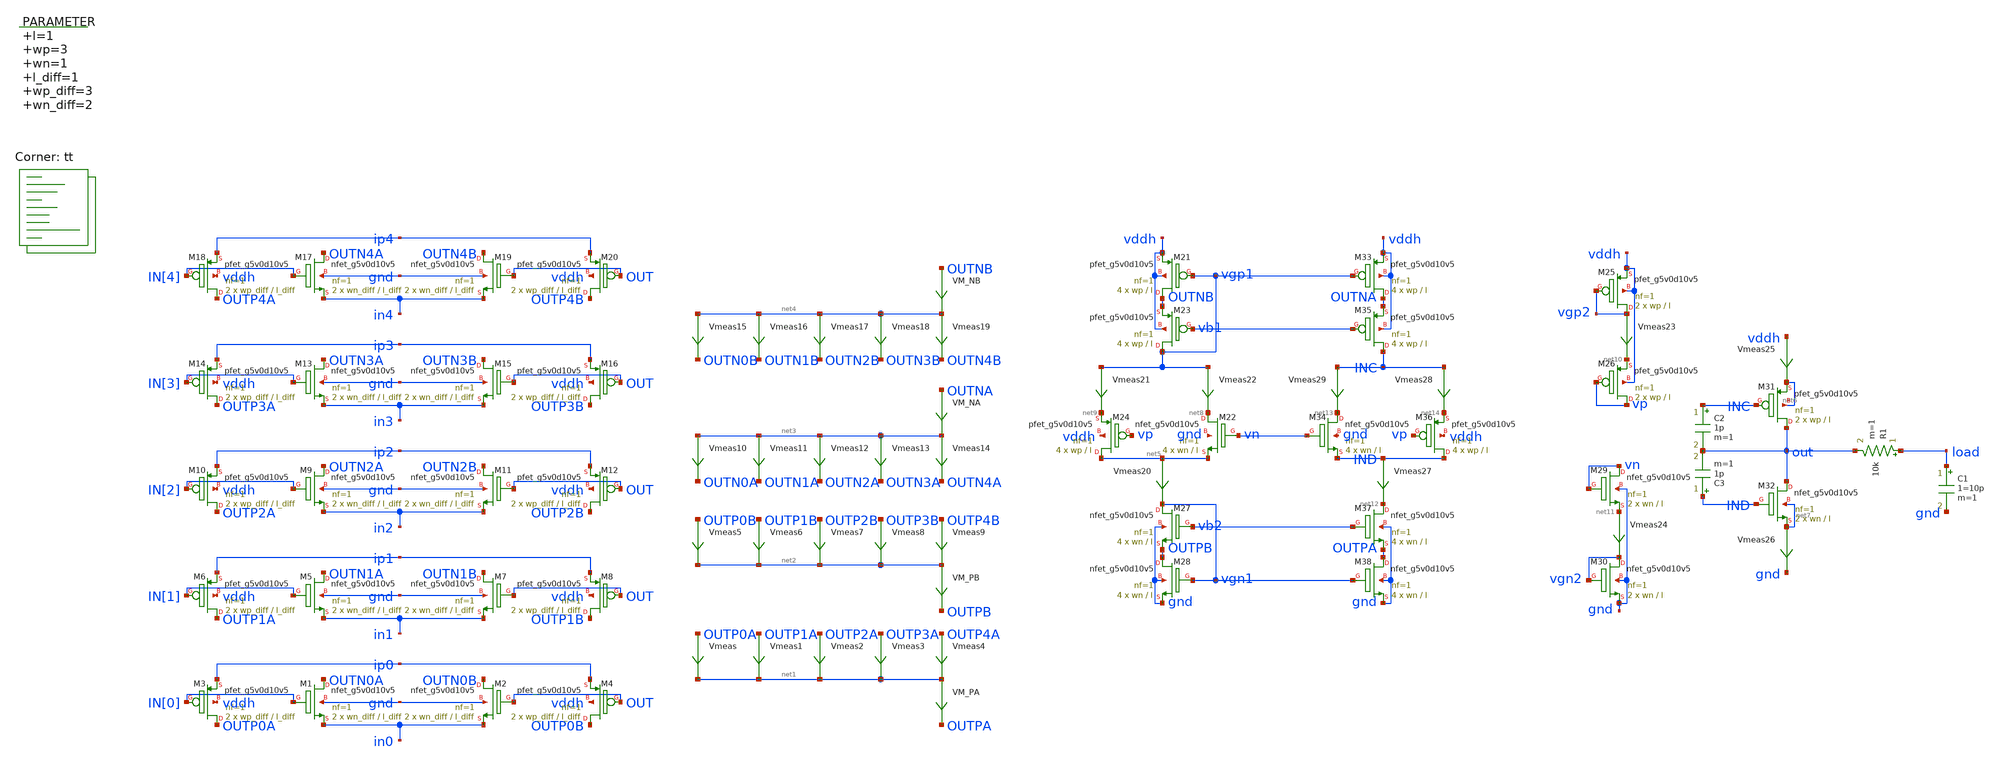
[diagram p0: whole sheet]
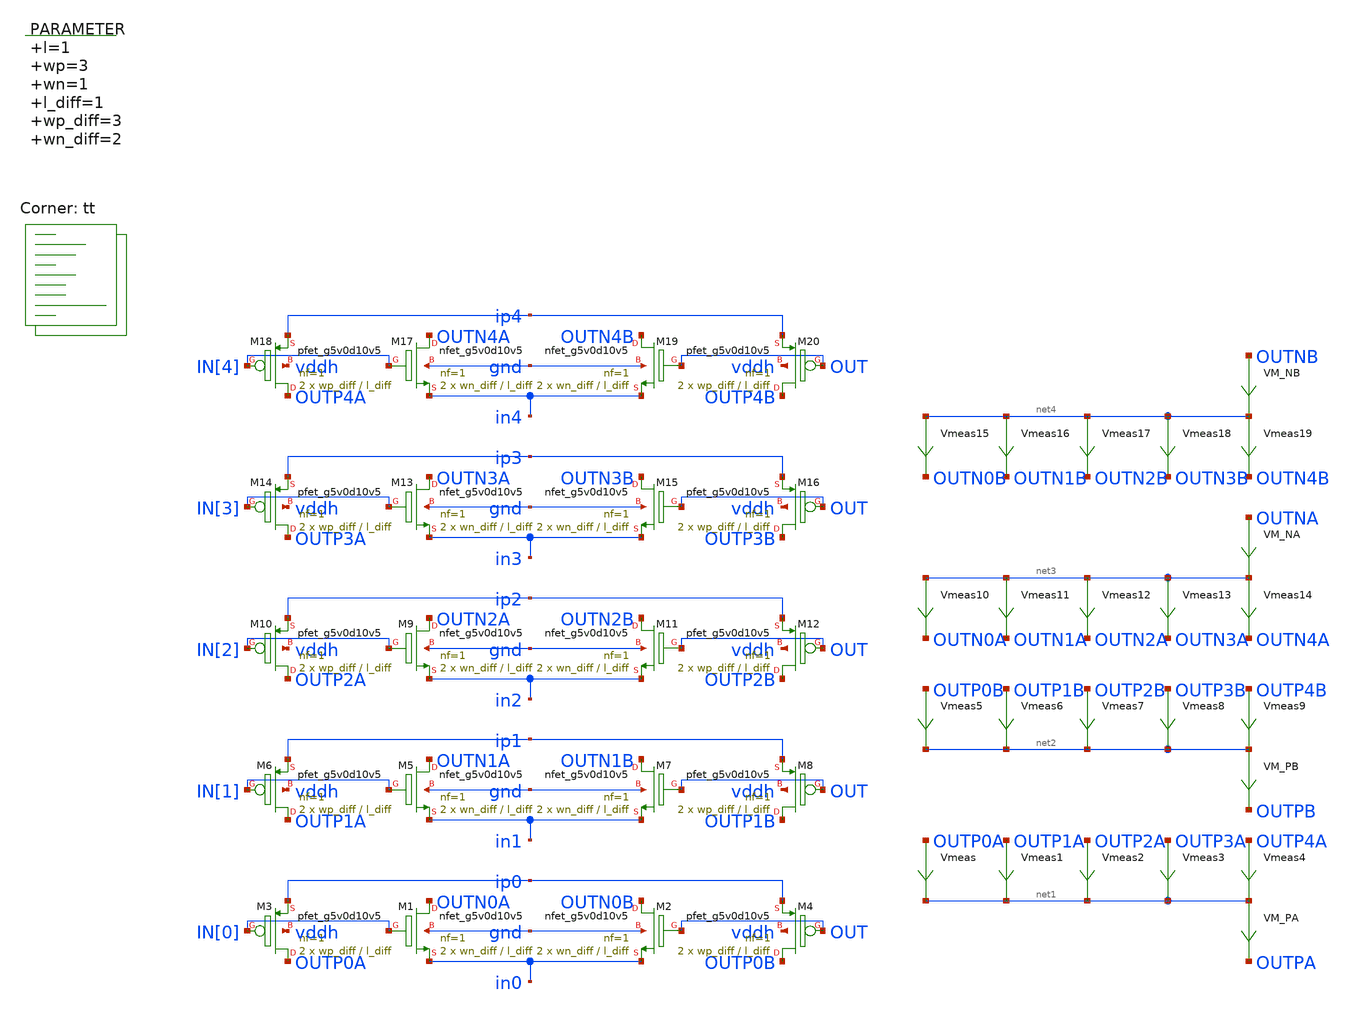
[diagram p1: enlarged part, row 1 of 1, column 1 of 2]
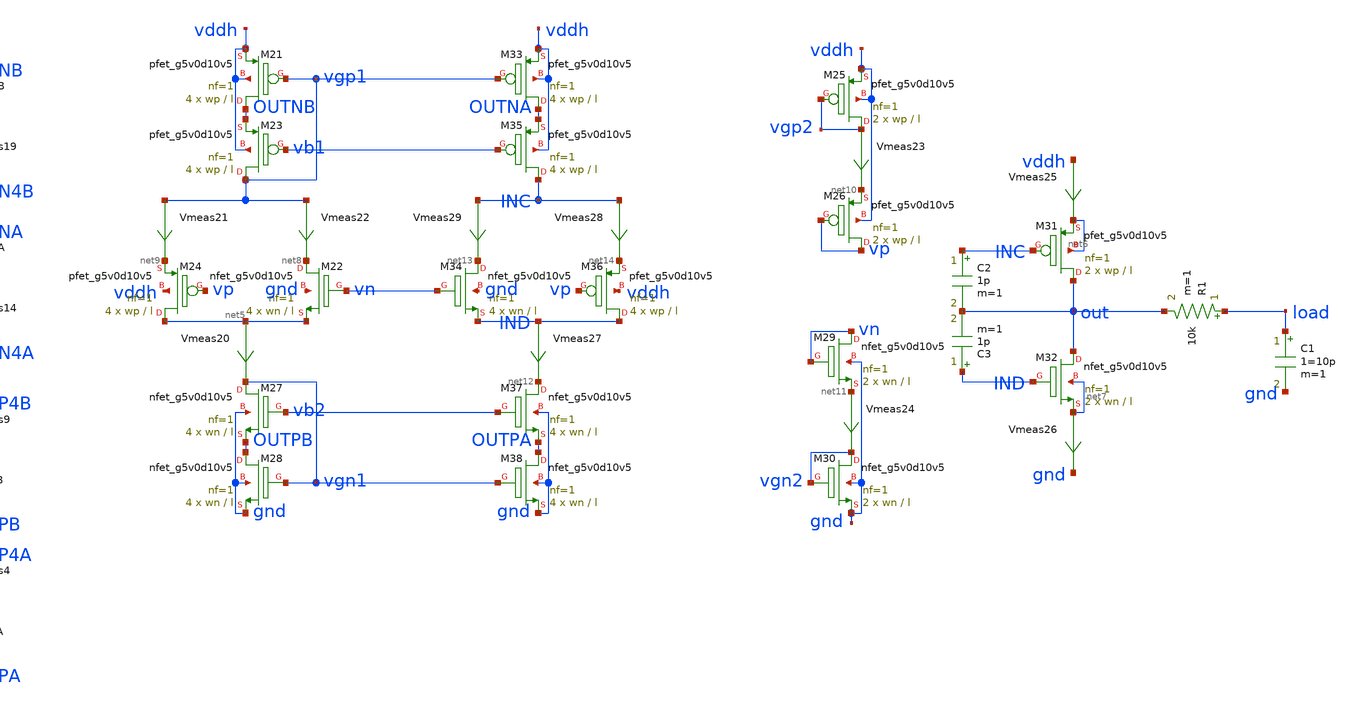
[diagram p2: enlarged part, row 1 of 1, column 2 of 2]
** sch_path: xschem/op_amp-tb.sch
**.subckt op_amp-tb
XM1 OUTN0A IN[0] in0 gnd sky130_fd_pr__nfet_g5v0d10v5 L=l_diff W=wn_diff nf=1 ad='int((nf+1)/2) * W/nf * 0.29'
+ as='int((nf+2)/2) * W/nf * 0.29' pd='2*int((nf+1)/2) * (W/nf + 0.29)' ps='2*int((nf+2)/2) * (W/nf + 0.29)'
+ nrd='0.29 / W' nrs='0.29 / W' sa=0 sb=0 sd=0 mult=2 m=2
XM3 OUTP0A IN[0] ip0 vddh sky130_fd_pr__pfet_g5v0d10v5 L=l_diff W=wp_diff nf=1 ad='int((nf+1)/2) * W/nf * 0.29'
+ as='int((nf+2)/2) * W/nf * 0.29' pd='2*int((nf+1)/2) * (W/nf + 0.29)' ps='2*int((nf+2)/2) * (W/nf + 0.29)'
+ nrd='0.29 / W' nrs='0.29 / W' sa=0 sb=0 sd=0 mult=2 m=2
Vmeas OUTP0A net1 0
.save i(vmeas)
Vmeas1 OUTP1A net1 0
.save i(vmeas1)
Vmeas2 OUTP2A net1 0
.save i(vmeas2)
Vmeas3 OUTP3A net1 0
.save i(vmeas3)
Vmeas4 OUTP4A net1 0
.save i(vmeas4)
Vmeas5 OUTP0B net2 0
.save i(vmeas5)
Vmeas6 OUTP1B net2 0
.save i(vmeas6)
Vmeas7 OUTP2B net2 0
.save i(vmeas7)
Vmeas8 OUTP3B net2 0
.save i(vmeas8)
Vmeas9 OUTP4B net2 0
.save i(vmeas9)
Vmeas10 net3 OUTN0A 0
.save i(vmeas10)
Vmeas11 net3 OUTN1A 0
.save i(vmeas11)
Vmeas12 net3 OUTN2A 0
.save i(vmeas12)
Vmeas13 net3 OUTN3A 0
.save i(vmeas13)
Vmeas14 net3 OUTN4A 0
.save i(vmeas14)
Vmeas15 net4 OUTN0B 0
.save i(vmeas15)
Vmeas16 net4 OUTN1B 0
.save i(vmeas16)
Vmeas17 net4 OUTN2B 0
.save i(vmeas17)
Vmeas18 net4 OUTN3B 0
.save i(vmeas18)
Vmeas19 net4 OUTN4B 0
.save i(vmeas19)
.param l=1 wp=3 wn=1 l_diff=1 wp_diff=3 wn_diff=2
Vmeas20 net5 vgn1 0
.save i(vmeas20)
XM21 OUTNB vgp1 vddh vddh sky130_fd_pr__pfet_g5v0d10v5 L=l W=wp nf=1 ad='int((nf+1)/2) * W/nf * 0.29'
+ as='int((nf+2)/2) * W/nf * 0.29' pd='2*int((nf+1)/2) * (W/nf + 0.29)' ps='2*int((nf+2)/2) * (W/nf + 0.29)'
+ nrd='0.29 / W' nrs='0.29 / W' sa=0 sb=0 sd=0 mult=4 m=4
XM22 net8 vn net5 gnd sky130_fd_pr__nfet_g5v0d10v5 L=l W=wn nf=1 ad='int((nf+1)/2) * W/nf * 0.29' as='int((nf+2)/2) * W/nf * 0.29'
+ pd='2*int((nf+1)/2) * (W/nf + 0.29)' ps='2*int((nf+2)/2) * (W/nf + 0.29)' nrd='0.29 / W' nrs='0.29 / W'
+ sa=0 sb=0 sd=0 mult=4 m=4
Vmeas21 vgp1 net9 0
.save i(vmeas21)
Vmeas22 vgp1 net8 0
.save i(vmeas22)
Vmeas23 vgp2 net10 0
.save i(vmeas23)
Vmeas24 net11 vgn2 0
.save i(vmeas24)
XM23 vgp1 vb1 OUTNB vddh sky130_fd_pr__pfet_g5v0d10v5 L=l W=wp nf=1 ad='int((nf+1)/2) * W/nf * 0.29'
+ as='int((nf+2)/2) * W/nf * 0.29' pd='2*int((nf+1)/2) * (W/nf + 0.29)' ps='2*int((nf+2)/2) * (W/nf + 0.29)'
+ nrd='0.29 / W' nrs='0.29 / W' sa=0 sb=0 sd=0 mult=4 m=4
XM24 net5 vp net9 vddh sky130_fd_pr__pfet_g5v0d10v5 L=l W=wp nf=1 ad='int((nf+1)/2) * W/nf * 0.29' as='int((nf+2)/2) * W/nf * 0.29'
+ pd='2*int((nf+1)/2) * (W/nf + 0.29)' ps='2*int((nf+2)/2) * (W/nf + 0.29)' nrd='0.29 / W' nrs='0.29 / W'
+ sa=0 sb=0 sd=0 mult=4 m=4
XM25 vgp2 vgp2 vddh vddh sky130_fd_pr__pfet_g5v0d10v5 L=l W=wp nf=1 ad='int((nf+1)/2) * W/nf * 0.29'
+ as='int((nf+2)/2) * W/nf * 0.29' pd='2*int((nf+1)/2) * (W/nf + 0.29)' ps='2*int((nf+2)/2) * (W/nf + 0.29)'
+ nrd='0.29 / W' nrs='0.29 / W' sa=0 sb=0 sd=0 mult=2 m=2
XM26 vp vp net10 vddh sky130_fd_pr__pfet_g5v0d10v5 L=l W=wp nf=1 ad='int((nf+1)/2) * W/nf * 0.29' as='int((nf+2)/2) * W/nf * 0.29'
+ pd='2*int((nf+1)/2) * (W/nf + 0.29)' ps='2*int((nf+2)/2) * (W/nf + 0.29)' nrd='0.29 / W' nrs='0.29 / W'
+ sa=0 sb=0 sd=0 mult=2 m=2
XM27 vgn1 vb2 OUTPB gnd sky130_fd_pr__nfet_g5v0d10v5 L=l W=wn nf=1 ad='int((nf+1)/2) * W/nf * 0.29' as='int((nf+2)/2) * W/nf * 0.29'
+ pd='2*int((nf+1)/2) * (W/nf + 0.29)' ps='2*int((nf+2)/2) * (W/nf + 0.29)' nrd='0.29 / W' nrs='0.29 / W'
+ sa=0 sb=0 sd=0 mult=4 m=4
XM28 OUTPB vgn1 gnd gnd sky130_fd_pr__nfet_g5v0d10v5 L=l W=wn nf=1 ad='int((nf+1)/2) * W/nf * 0.29' as='int((nf+2)/2) * W/nf * 0.29'
+ pd='2*int((nf+1)/2) * (W/nf + 0.29)' ps='2*int((nf+2)/2) * (W/nf + 0.29)' nrd='0.29 / W' nrs='0.29 / W'
+ sa=0 sb=0 sd=0 mult=4 m=4
XM29 vn vn net11 gnd sky130_fd_pr__nfet_g5v0d10v5 L=l W=wn nf=1 ad='int((nf+1)/2) * W/nf * 0.29' as='int((nf+2)/2) * W/nf * 0.29'
+ pd='2*int((nf+1)/2) * (W/nf + 0.29)' ps='2*int((nf+2)/2) * (W/nf + 0.29)' nrd='0.29 / W' nrs='0.29 / W'
+ sa=0 sb=0 sd=0 mult=2 m=2
XM30 vgn2 vgn2 gnd gnd sky130_fd_pr__nfet_g5v0d10v5 L=l W=wn nf=1 ad='int((nf+1)/2) * W/nf * 0.29' as='int((nf+2)/2) * W/nf * 0.29'
+ pd='2*int((nf+1)/2) * (W/nf + 0.29)' ps='2*int((nf+2)/2) * (W/nf + 0.29)' nrd='0.29 / W' nrs='0.29 / W'
+ sa=0 sb=0 sd=0 mult=2 m=2
XM31 out INC net6 net6 sky130_fd_pr__pfet_g5v0d10v5 L=l W=wp nf=1 ad='int((nf+1)/2) * W/nf * 0.29' as='int((nf+2)/2) * W/nf * 0.29'
+ pd='2*int((nf+1)/2) * (W/nf + 0.29)' ps='2*int((nf+2)/2) * (W/nf + 0.29)' nrd='0.29 / W' nrs='0.29 / W'
+ sa=0 sb=0 sd=0 mult=2 m=2
XM32 out IND net7 net7 sky130_fd_pr__nfet_g5v0d10v5 L=l W=wn nf=1 ad='int((nf+1)/2) * W/nf * 0.29' as='int((nf+2)/2) * W/nf * 0.29'
+ pd='2*int((nf+1)/2) * (W/nf + 0.29)' ps='2*int((nf+2)/2) * (W/nf + 0.29)' nrd='0.29 / W' nrs='0.29 / W'
+ sa=0 sb=0 sd=0 mult=2 m=2
R1 load out 10k m=1
Vmeas25 vddh net6 0
.save i(vmeas25)
Vmeas26 net7 gnd 0
.save i(vmeas26)
C1 load gnd 1=10p m=1
Vmeas27 IND net12 0
.save i(vmeas27)
XM33 OUTNA vgp1 vddh vddh sky130_fd_pr__pfet_g5v0d10v5 L=l W=wp nf=1 ad='int((nf+1)/2) * W/nf * 0.29'
+ as='int((nf+2)/2) * W/nf * 0.29' pd='2*int((nf+1)/2) * (W/nf + 0.29)' ps='2*int((nf+2)/2) * (W/nf + 0.29)'
+ nrd='0.29 / W' nrs='0.29 / W' sa=0 sb=0 sd=0 mult=4 m=4
XM34 net13 vn IND gnd sky130_fd_pr__nfet_g5v0d10v5 L=l W=wn nf=1 ad='int((nf+1)/2) * W/nf * 0.29' as='int((nf+2)/2) * W/nf * 0.29'
+ pd='2*int((nf+1)/2) * (W/nf + 0.29)' ps='2*int((nf+2)/2) * (W/nf + 0.29)' nrd='0.29 / W' nrs='0.29 / W'
+ sa=0 sb=0 sd=0 mult=4 m=4
Vmeas28 INC net14 0
.save i(vmeas28)
Vmeas29 INC net13 0
.save i(vmeas29)
XM35 INC vb1 OUTNA vddh sky130_fd_pr__pfet_g5v0d10v5 L=l W=wp nf=1 ad='int((nf+1)/2) * W/nf * 0.29' as='int((nf+2)/2) * W/nf * 0.29'
+ pd='2*int((nf+1)/2) * (W/nf + 0.29)' ps='2*int((nf+2)/2) * (W/nf + 0.29)' nrd='0.29 / W' nrs='0.29 / W'
+ sa=0 sb=0 sd=0 mult=4 m=4
XM36 IND vp net14 vddh sky130_fd_pr__pfet_g5v0d10v5 L=l W=wp nf=1 ad='int((nf+1)/2) * W/nf * 0.29' as='int((nf+2)/2) * W/nf * 0.29'
+ pd='2*int((nf+1)/2) * (W/nf + 0.29)' ps='2*int((nf+2)/2) * (W/nf + 0.29)' nrd='0.29 / W' nrs='0.29 / W'
+ sa=0 sb=0 sd=0 mult=4 m=4
XM37 net12 vb2 OUTPA gnd sky130_fd_pr__nfet_g5v0d10v5 L=l W=wn nf=1 ad='int((nf+1)/2) * W/nf * 0.29'
+ as='int((nf+2)/2) * W/nf * 0.29' pd='2*int((nf+1)/2) * (W/nf + 0.29)' ps='2*int((nf+2)/2) * (W/nf + 0.29)'
+ nrd='0.29 / W' nrs='0.29 / W' sa=0 sb=0 sd=0 mult=4 m=4
XM38 OUTPA vgn1 gnd gnd sky130_fd_pr__nfet_g5v0d10v5 L=l W=wn nf=1 ad='int((nf+1)/2) * W/nf * 0.29' as='int((nf+2)/2) * W/nf * 0.29'
+ pd='2*int((nf+1)/2) * (W/nf + 0.29)' ps='2*int((nf+2)/2) * (W/nf + 0.29)' nrd='0.29 / W' nrs='0.29 / W'
+ sa=0 sb=0 sd=0 mult=4 m=4
VM_NB OUTNB net4 0
.save i(vm_nb)
VM_NA OUTNA net3 0
.save i(vm_na)
VM_PB net2 OUTPB 0
.save i(vm_pb)
VM_PA net1 OUTPA 0
.save i(vm_pa)
C2 INC out 1p m=1
C3 IND out 1p m=1
XM2 OUTN0B OUT in0 gnd sky130_fd_pr__nfet_g5v0d10v5 L=l_diff W=wn_diff nf=1 ad='int((nf+1)/2) * W/nf * 0.29'
+ as='int((nf+2)/2) * W/nf * 0.29' pd='2*int((nf+1)/2) * (W/nf + 0.29)' ps='2*int((nf+2)/2) * (W/nf + 0.29)'
+ nrd='0.29 / W' nrs='0.29 / W' sa=0 sb=0 sd=0 mult=2 m=2
XM4 OUTP0B OUT ip0 vddh sky130_fd_pr__pfet_g5v0d10v5 L=l_diff W=wp_diff nf=1 ad='int((nf+1)/2) * W/nf * 0.29'
+ as='int((nf+2)/2) * W/nf * 0.29' pd='2*int((nf+1)/2) * (W/nf + 0.29)' ps='2*int((nf+2)/2) * (W/nf + 0.29)'
+ nrd='0.29 / W' nrs='0.29 / W' sa=0 sb=0 sd=0 mult=2 m=2
XM5 OUTN1A IN[1] in1 gnd sky130_fd_pr__nfet_g5v0d10v5 L=l_diff W=wn_diff nf=1 ad='int((nf+1)/2) * W/nf * 0.29'
+ as='int((nf+2)/2) * W/nf * 0.29' pd='2*int((nf+1)/2) * (W/nf + 0.29)' ps='2*int((nf+2)/2) * (W/nf + 0.29)'
+ nrd='0.29 / W' nrs='0.29 / W' sa=0 sb=0 sd=0 mult=2 m=2
XM6 OUTP1A IN[1] ip1 vddh sky130_fd_pr__pfet_g5v0d10v5 L=l_diff W=wp_diff nf=1 ad='int((nf+1)/2) * W/nf * 0.29'
+ as='int((nf+2)/2) * W/nf * 0.29' pd='2*int((nf+1)/2) * (W/nf + 0.29)' ps='2*int((nf+2)/2) * (W/nf + 0.29)'
+ nrd='0.29 / W' nrs='0.29 / W' sa=0 sb=0 sd=0 mult=2 m=2
XM7 OUTN1B OUT in1 gnd sky130_fd_pr__nfet_g5v0d10v5 L=l_diff W=wn_diff nf=1 ad='int((nf+1)/2) * W/nf * 0.29'
+ as='int((nf+2)/2) * W/nf * 0.29' pd='2*int((nf+1)/2) * (W/nf + 0.29)' ps='2*int((nf+2)/2) * (W/nf + 0.29)'
+ nrd='0.29 / W' nrs='0.29 / W' sa=0 sb=0 sd=0 mult=2 m=2
XM8 OUTP1B OUT ip1 vddh sky130_fd_pr__pfet_g5v0d10v5 L=l_diff W=wp_diff nf=1 ad='int((nf+1)/2) * W/nf * 0.29'
+ as='int((nf+2)/2) * W/nf * 0.29' pd='2*int((nf+1)/2) * (W/nf + 0.29)' ps='2*int((nf+2)/2) * (W/nf + 0.29)'
+ nrd='0.29 / W' nrs='0.29 / W' sa=0 sb=0 sd=0 mult=2 m=2
XM9 OUTN2A IN[2] in2 gnd sky130_fd_pr__nfet_g5v0d10v5 L=l_diff W=wn_diff nf=1 ad='int((nf+1)/2) * W/nf * 0.29'
+ as='int((nf+2)/2) * W/nf * 0.29' pd='2*int((nf+1)/2) * (W/nf + 0.29)' ps='2*int((nf+2)/2) * (W/nf + 0.29)'
+ nrd='0.29 / W' nrs='0.29 / W' sa=0 sb=0 sd=0 mult=2 m=2
XM10 OUTP2A IN[2] ip2 vddh sky130_fd_pr__pfet_g5v0d10v5 L=l_diff W=wp_diff nf=1 ad='int((nf+1)/2) * W/nf * 0.29'
+ as='int((nf+2)/2) * W/nf * 0.29' pd='2*int((nf+1)/2) * (W/nf + 0.29)' ps='2*int((nf+2)/2) * (W/nf + 0.29)'
+ nrd='0.29 / W' nrs='0.29 / W' sa=0 sb=0 sd=0 mult=2 m=2
XM11 OUTN2B OUT in2 gnd sky130_fd_pr__nfet_g5v0d10v5 L=l_diff W=wn_diff nf=1 ad='int((nf+1)/2) * W/nf * 0.29'
+ as='int((nf+2)/2) * W/nf * 0.29' pd='2*int((nf+1)/2) * (W/nf + 0.29)' ps='2*int((nf+2)/2) * (W/nf + 0.29)'
+ nrd='0.29 / W' nrs='0.29 / W' sa=0 sb=0 sd=0 mult=2 m=2
XM12 OUTP2B OUT ip2 vddh sky130_fd_pr__pfet_g5v0d10v5 L=l_diff W=wp_diff nf=1 ad='int((nf+1)/2) * W/nf * 0.29'
+ as='int((nf+2)/2) * W/nf * 0.29' pd='2*int((nf+1)/2) * (W/nf + 0.29)' ps='2*int((nf+2)/2) * (W/nf + 0.29)'
+ nrd='0.29 / W' nrs='0.29 / W' sa=0 sb=0 sd=0 mult=2 m=2
XM13 OUTN3A IN[3] in3 gnd sky130_fd_pr__nfet_g5v0d10v5 L=l_diff W=wn_diff nf=1 ad='int((nf+1)/2) * W/nf * 0.29'
+ as='int((nf+2)/2) * W/nf * 0.29' pd='2*int((nf+1)/2) * (W/nf + 0.29)' ps='2*int((nf+2)/2) * (W/nf + 0.29)'
+ nrd='0.29 / W' nrs='0.29 / W' sa=0 sb=0 sd=0 mult=2 m=2
XM14 OUTP3A IN[3] ip3 vddh sky130_fd_pr__pfet_g5v0d10v5 L=l_diff W=wp_diff nf=1 ad='int((nf+1)/2) * W/nf * 0.29'
+ as='int((nf+2)/2) * W/nf * 0.29' pd='2*int((nf+1)/2) * (W/nf + 0.29)' ps='2*int((nf+2)/2) * (W/nf + 0.29)'
+ nrd='0.29 / W' nrs='0.29 / W' sa=0 sb=0 sd=0 mult=2 m=2
XM15 OUTN3B OUT in3 gnd sky130_fd_pr__nfet_g5v0d10v5 L=l_diff W=wn_diff nf=1 ad='int((nf+1)/2) * W/nf * 0.29'
+ as='int((nf+2)/2) * W/nf * 0.29' pd='2*int((nf+1)/2) * (W/nf + 0.29)' ps='2*int((nf+2)/2) * (W/nf + 0.29)'
+ nrd='0.29 / W' nrs='0.29 / W' sa=0 sb=0 sd=0 mult=2 m=2
XM16 OUTP3B OUT ip3 vddh sky130_fd_pr__pfet_g5v0d10v5 L=l_diff W=wp_diff nf=1 ad='int((nf+1)/2) * W/nf * 0.29'
+ as='int((nf+2)/2) * W/nf * 0.29' pd='2*int((nf+1)/2) * (W/nf + 0.29)' ps='2*int((nf+2)/2) * (W/nf + 0.29)'
+ nrd='0.29 / W' nrs='0.29 / W' sa=0 sb=0 sd=0 mult=2 m=2
XM17 OUTN4A IN[4] in4 gnd sky130_fd_pr__nfet_g5v0d10v5 L=l_diff W=wn_diff nf=1 ad='int((nf+1)/2) * W/nf * 0.29'
+ as='int((nf+2)/2) * W/nf * 0.29' pd='2*int((nf+1)/2) * (W/nf + 0.29)' ps='2*int((nf+2)/2) * (W/nf + 0.29)'
+ nrd='0.29 / W' nrs='0.29 / W' sa=0 sb=0 sd=0 mult=2 m=2
XM18 OUTP4A IN[4] ip4 vddh sky130_fd_pr__pfet_g5v0d10v5 L=l_diff W=wp_diff nf=1 ad='int((nf+1)/2) * W/nf * 0.29'
+ as='int((nf+2)/2) * W/nf * 0.29' pd='2*int((nf+1)/2) * (W/nf + 0.29)' ps='2*int((nf+2)/2) * (W/nf + 0.29)'
+ nrd='0.29 / W' nrs='0.29 / W' sa=0 sb=0 sd=0 mult=2 m=2
XM19 OUTN4B OUT in4 gnd sky130_fd_pr__nfet_g5v0d10v5 L=l_diff W=wn_diff nf=1 ad='int((nf+1)/2) * W/nf * 0.29'
+ as='int((nf+2)/2) * W/nf * 0.29' pd='2*int((nf+1)/2) * (W/nf + 0.29)' ps='2*int((nf+2)/2) * (W/nf + 0.29)'
+ nrd='0.29 / W' nrs='0.29 / W' sa=0 sb=0 sd=0 mult=2 m=2
XM20 OUTP4B OUT ip4 vddh sky130_fd_pr__pfet_g5v0d10v5 L=l_diff W=wp_diff nf=1 ad='int((nf+1)/2) * W/nf * 0.29'
+ as='int((nf+2)/2) * W/nf * 0.29' pd='2*int((nf+1)/2) * (W/nf + 0.29)' ps='2*int((nf+2)/2) * (W/nf + 0.29)'
+ nrd='0.29 / W' nrs='0.29 / W' sa=0 sb=0 sd=0 mult=2 m=2
**** begin user architecture code
.lib $::SKYWATER_MODELS/sky130.lib.spice tt



  .option wnflag=1
  .option safecurrents
  ********************Static Current Sources***************************
  .param base_current=0.1u
  .param i0=base_current i1={1*i0} i2={2*i0} i3={4*i0} i4={8*i0}
  Ip0 vddh ip0 i0
  In0 in0  gnd i0

  Ip1 vddh ip1 i1
  In1 in1  gnd i1

  Ip2 vddh ip2 i2
  In2 in2  gnd i2

  Ip3 vddh ip3 i3
  In3 in3  gnd i3

  Ip4 vddh ip4 i4
  In4 in4  gnd i4

  Ivp vp gnd 10u
  Ivn vddh vn 10u
  ********************Static Voltage Sources***************************
  Vddh vddh gnd dc 5.5

  vb1 vb1 gnd dc 3.37
  vb2 vb2 gnd dc 1.95

  vina ina gnd sin({5.5/2} {5.5/2} 100k)
  vinb inb gnd sin({5.5/2} {-5.5/2} 100k)

  .param vin_val=4.661
  *vin0 in[0] gnd dc vin_val
  *vin1 in[1] gnd dc vin_val
  *vin2 in[2] gnd dc vin_val
  *vin3 in[3] gnd dc vin_val
  *vin4 in[4] gnd dc vin_val
  ********************Dynamic Voltage Sources***************************
  *******Calculation**********
  .param base_f=100e3 base_t={1/base_f} base_th={base_t/2} base_d={base_th}
  .param b0_th={base_th} b0_t={b0_th*2}
  .param b1_th={b0_th*2} b1_t={b1_th*2}
  .param b2_th={b1_th*2} b2_t={b2_th*2}
  .param b3_th={b2_th*2} b3_t={b3_th*2}
  *******Signals**********
  .param vh=1.162 vl=1.044
  vin0 in[0] gnd dc vl
  Vin1 in[1] gnd pulse({vh} {vl} {base_d} 1n 1n {b0_th} {b0_t})
  Vin2 in[2] gnd pulse({vh} {vl} {base_d} 1n 1n {b1_th} {b1_t})
  Vin3 in[3] gnd pulse({vh} {vl} {base_d} 1n 1n {b2_th} {b2_t})
  Vin4 in[4] gnd pulse({vh} {vl} {base_d} 1n 1n {b3_th} {b3_t})
  ********************Simulation Commands*****************************
  .control
     reset
     save all
     tran 1n 150u
     *dc vin 0 5.5 0.001
     write op_amp-tb.raw
     wrdata /home/yohanes/10-bit-DAC/simulations/op_amp-tb.txt out load
     set appendwrite
*    quit 0
  .endc



**** end user architecture code
**.ends
.end
